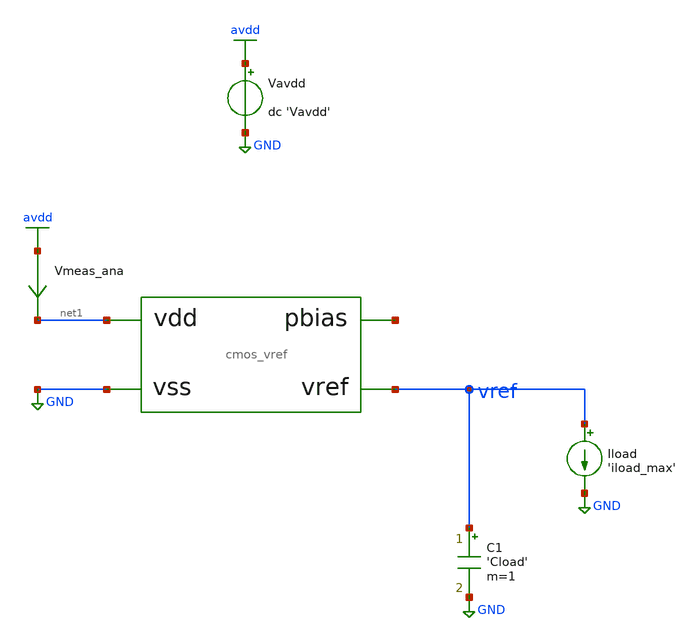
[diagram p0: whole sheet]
** sch_path: tb/cmos_vref/tb_vref_load_reg.sch
**.subckt tb_vref_load_reg
Vavdd avdd GND dc 'Vavdd'
C1 vref GND 'Cload' m=1
Vmeas_ana avdd net1 0
.save i(vmeas_ana)
X1 vref net1 GND net2 cmos_vref
Iload vref GND 'iload_max'
**** begin user architecture code


.lib 'models_dir'/cornerMOShv.lib 'mos_corner'
.lib 'models_dir'/cornerMOSlv.lib 'mos_corner'
.lib 'models_dir'/cornerCAP.lib cap_typ
.option TEMP='temperature'
.option warn=1
.control
save vref
dc Iload 'iload_min' 'iload_max' 1n
set wr_singlescale
wrdata 'simpath'/'filename'_'N'.data V(vref)
quit
.endc


**** end user architecture code
**.ends
.GLOBAL avdd
.GLOBAL GND
.end
